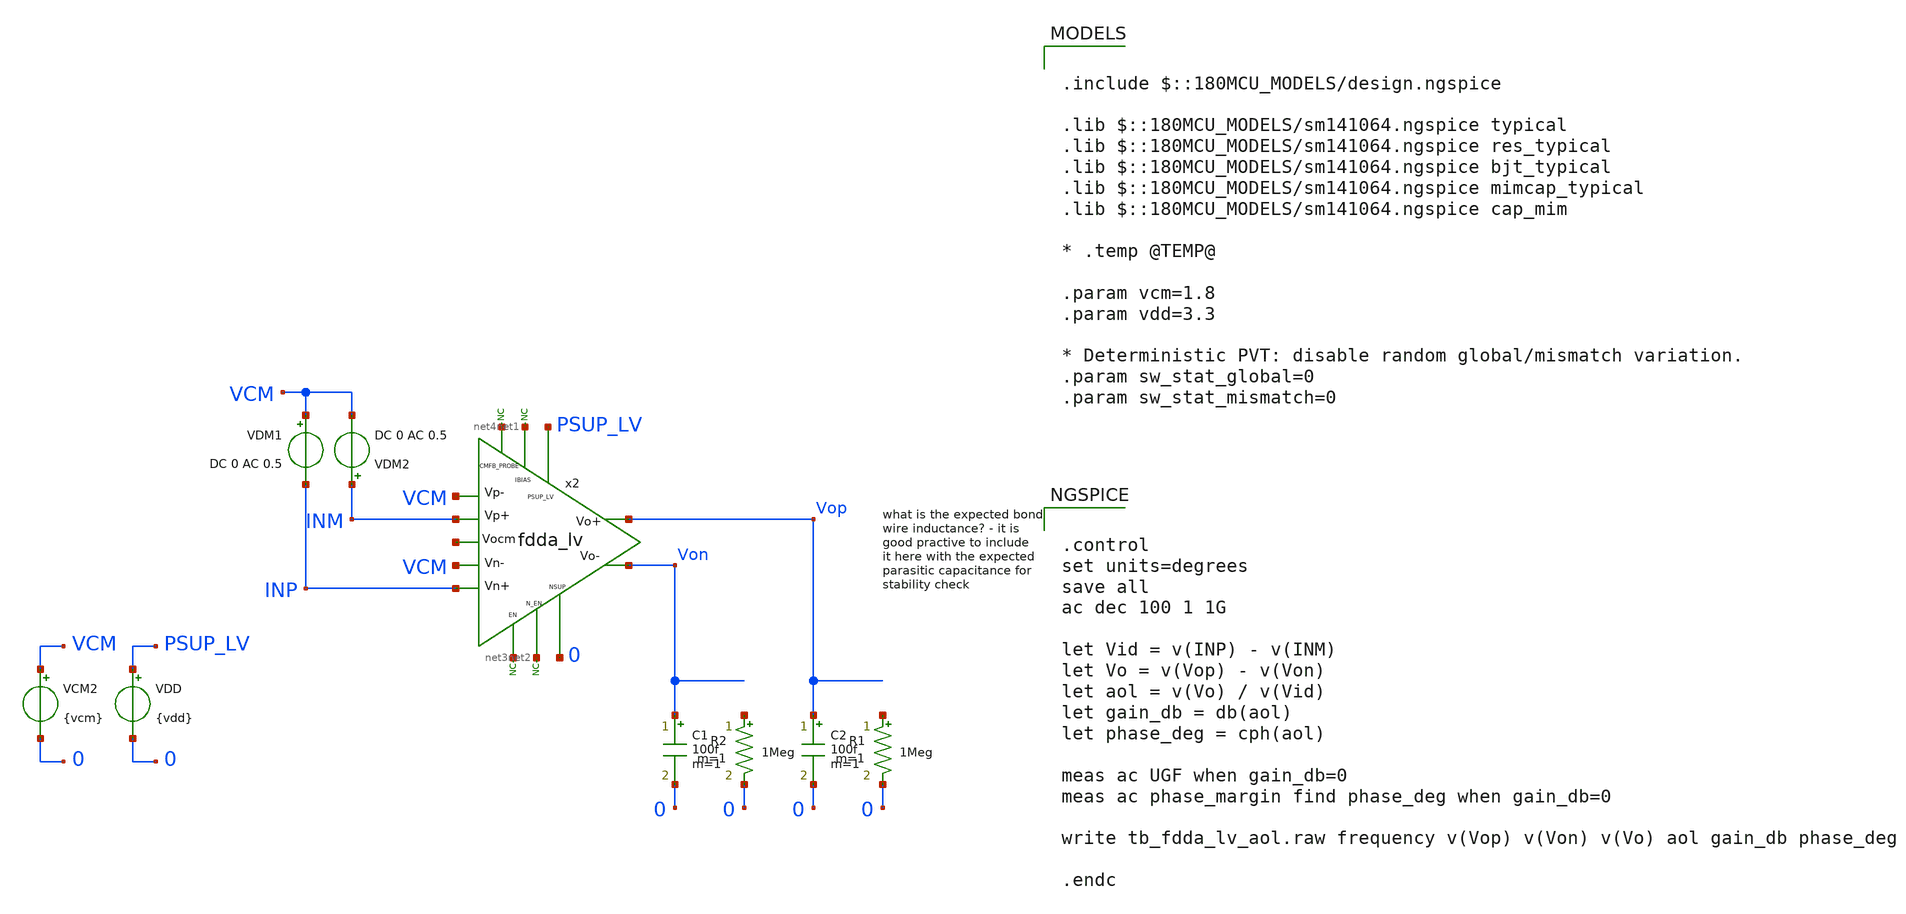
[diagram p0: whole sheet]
** sch_path: xschem/blocks/fdda_lv/tb_fdda_lv_aol.sch
**.subckt tb_fdda_lv_aol
C1 Von 0 100f m=1
x2 PSUP_LV VCM VCM INP INM Vop Von net1 net2 net3 0 net4 net5 fdda_lv
* noconn #net1
* noconn #net3
* noconn #net2
VDD PSUP_LV 0 {vdd}
C2 Vop 0 100f m=1
VCM2 VCM 0 {vcm}
VDM2 INM VCM DC 0 AC 0.5
VDM1 VCM INP DC 0 AC 0.5
* noconn #net4
R1 net6 0 1Meg m=1
R2 net7 0 1Meg m=1
**** begin user architecture code

.include $::180MCU_MODELS/design.ngspice

.lib $::180MCU_MODELS/sm141064.ngspice typical
.lib $::180MCU_MODELS/sm141064.ngspice res_typical
.lib $::180MCU_MODELS/sm141064.ngspice bjt_typical
.lib $::180MCU_MODELS/sm141064.ngspice mimcap_typical
.lib $::180MCU_MODELS/sm141064.ngspice cap_mim

* .temp @TEMP@

.param vcm=1.8
.param vdd=3.3

* Deterministic PVT: disable random global/mismatch variation.
.param sw_stat_global=0
.param sw_stat_mismatch=0



.control
set units=degrees
save all
ac dec 100 1 1G

let Vid = v(INP) - v(INM)
let Vo = v(Vop) - v(Von)
let aol = v(Vo) / v(Vid)
let gain_db = db(aol)
let phase_deg = cph(aol)

meas ac UGF when gain_db=0
meas ac phase_margin find phase_deg when gain_db=0

write tb_fdda_lv_aol.raw frequency v(Vop) v(Von) v(Vo) aol gain_db phase_deg

.endc


**** end user architecture code
**.ends
.end
